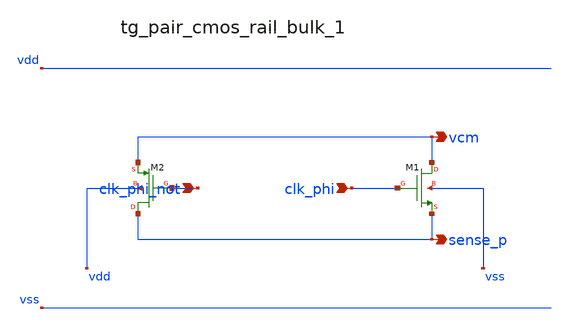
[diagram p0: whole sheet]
** sch_path: analog-db/raw/cmfb_004_output_switched_cap/hier/blocks/tg_pair_cmos_rail_bulk_1.sch
**.subckt tg_pair_cmos_rail_bulk_1 clk_phi_not clk_phi vcm sense_p
*.ipin clk_phi_not
*.ipin clk_phi
*.opin vcm
*.opin sense_p
XM1 vcm clk_phi sense_p vss sg13_lv_nmos w=x_dut_xm1_w l=x_dut_xm1_l ng=1 m=x_dut_xm1_m
XM2 sense_p clk_phi_not vcm vdd sg13_lv_pmos w=x_dut_xm2_w l=x_dut_xm2_l ng=1 m=x_dut_xm2_m
**.ends
.end
